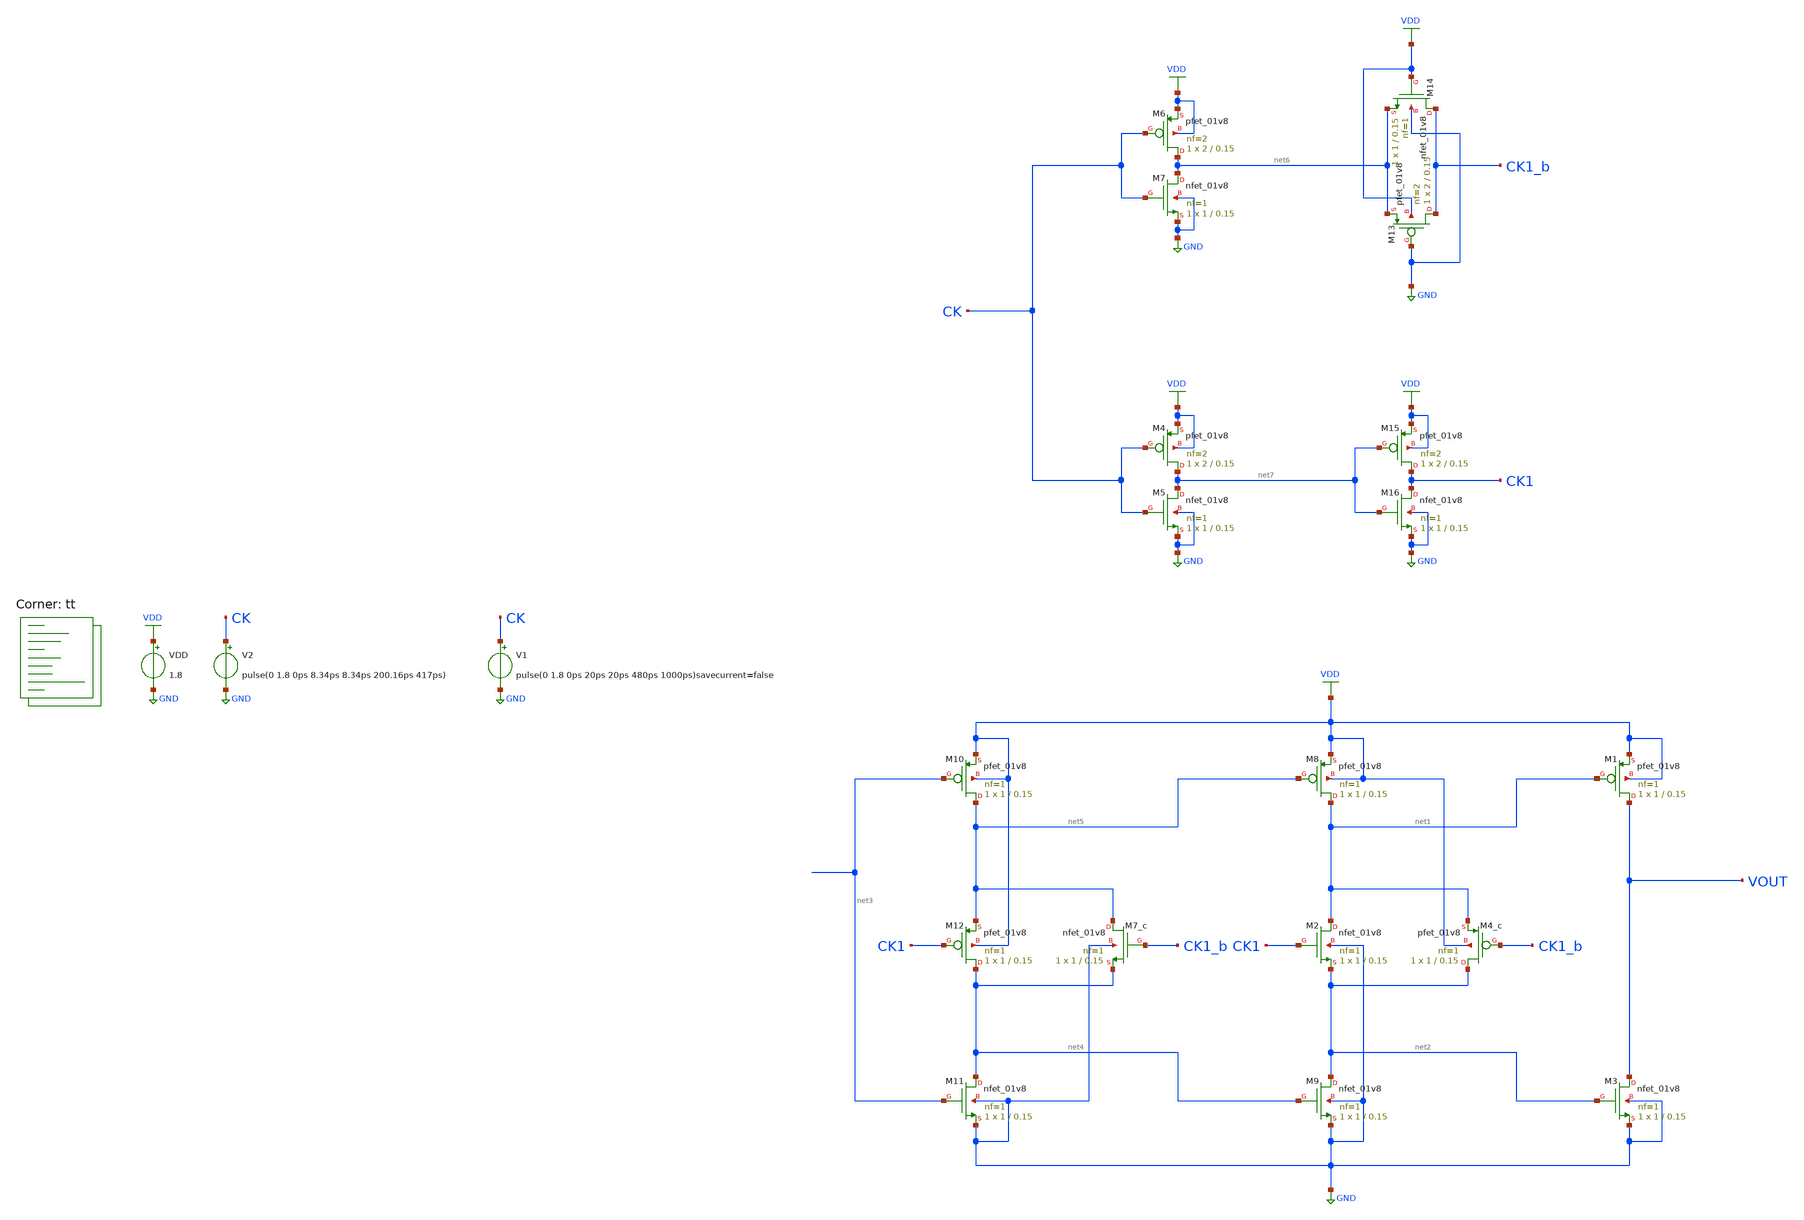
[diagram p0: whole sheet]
** sch_path: projects/pll/divider/xschem_ngspice/tb_FF_comp_sw_divide2_2.sch
**.subckt tb_FF_comp_sw_divide2_2
VDD VDD GND 1.8
V2 CK GND pulse(0 1.8 0ps 8.34ps 8.34ps 200.16ps 417ps)
XM1 VOUT net1 VDD VDD sky130_fd_pr__pfet_01v8 L=0.15 W=1 nf=1 ad='int((nf+1)/2) * W/nf * 0.29' as='int((nf+2)/2) * W/nf * 0.29'
+ pd='2*int((nf+1)/2) * (W/nf + 0.29)' ps='2*int((nf+2)/2) * (W/nf + 0.29)' nrd='0.29 / W' nrs='0.29 / W'
+ sa=0 sb=0 sd=0 mult=1 m=1
XM2 net1 CK1 net2 GND sky130_fd_pr__nfet_01v8 L=0.15 W=1 nf=1 ad='int((nf+1)/2) * W/nf * 0.29' as='int((nf+2)/2) * W/nf * 0.29'
+ pd='2*int((nf+1)/2) * (W/nf + 0.29)' ps='2*int((nf+2)/2) * (W/nf + 0.29)' nrd='0.29 / W' nrs='0.29 / W'
+ sa=0 sb=0 sd=0 mult=1 m=1
XM3 VOUT net2 GND GND sky130_fd_pr__nfet_01v8 L=0.15 W=1 nf=1 ad='int((nf+1)/2) * W/nf * 0.29' as='int((nf+2)/2) * W/nf * 0.29'
+ pd='2*int((nf+1)/2) * (W/nf + 0.29)' ps='2*int((nf+2)/2) * (W/nf + 0.29)' nrd='0.29 / W' nrs='0.29 / W'
+ sa=0 sb=0 sd=0 mult=1 m=1
XM8 net1 net5 VDD VDD sky130_fd_pr__pfet_01v8 L=0.15 W=1 nf=1 ad='int((nf+1)/2) * W/nf * 0.29' as='int((nf+2)/2) * W/nf * 0.29'
+ pd='2*int((nf+1)/2) * (W/nf + 0.29)' ps='2*int((nf+2)/2) * (W/nf + 0.29)' nrd='0.29 / W' nrs='0.29 / W'
+ sa=0 sb=0 sd=0 mult=1 m=1
XM9 net2 net4 GND GND sky130_fd_pr__nfet_01v8 L=0.15 W=1 nf=1 ad='int((nf+1)/2) * W/nf * 0.29' as='int((nf+2)/2) * W/nf * 0.29'
+ pd='2*int((nf+1)/2) * (W/nf + 0.29)' ps='2*int((nf+2)/2) * (W/nf + 0.29)' nrd='0.29 / W' nrs='0.29 / W'
+ sa=0 sb=0 sd=0 mult=1 m=1
XM10 net5 net3 VDD VDD sky130_fd_pr__pfet_01v8 L=0.15 W=1 nf=1 ad='int((nf+1)/2) * W/nf * 0.29' as='int((nf+2)/2) * W/nf * 0.29'
+ pd='2*int((nf+1)/2) * (W/nf + 0.29)' ps='2*int((nf+2)/2) * (W/nf + 0.29)' nrd='0.29 / W' nrs='0.29 / W'
+ sa=0 sb=0 sd=0 mult=1 m=1
XM11 net4 net3 GND GND sky130_fd_pr__nfet_01v8 L=0.15 W=1 nf=1 ad='int((nf+1)/2) * W/nf * 0.29' as='int((nf+2)/2) * W/nf * 0.29'
+ pd='2*int((nf+1)/2) * (W/nf + 0.29)' ps='2*int((nf+2)/2) * (W/nf + 0.29)' nrd='0.29 / W' nrs='0.29 / W'
+ sa=0 sb=0 sd=0 mult=1 m=1
XM12 net4 CK1 net5 VDD sky130_fd_pr__pfet_01v8 L=0.15 W=1 nf=1 ad='int((nf+1)/2) * W/nf * 0.29' as='int((nf+2)/2) * W/nf * 0.29'
+ pd='2*int((nf+1)/2) * (W/nf + 0.29)' ps='2*int((nf+2)/2) * (W/nf + 0.29)' nrd='0.29 / W' nrs='0.29 / W'
+ sa=0 sb=0 sd=0 mult=1 m=1
XM4_c net2 CK1_b net1 VDD sky130_fd_pr__pfet_01v8 L=0.15 W=1 nf=1 ad='int((nf+1)/2) * W/nf * 0.29' as='int((nf+2)/2) * W/nf * 0.29'
+ pd='2*int((nf+1)/2) * (W/nf + 0.29)' ps='2*int((nf+2)/2) * (W/nf + 0.29)' nrd='0.29 / W' nrs='0.29 / W'
+ sa=0 sb=0 sd=0 mult=1 m=1
XM7_c net5 CK1_b net4 GND sky130_fd_pr__nfet_01v8 L=0.15 W=1 nf=1 ad='int((nf+1)/2) * W/nf * 0.29' as='int((nf+2)/2) * W/nf * 0.29'
+ pd='2*int((nf+1)/2) * (W/nf + 0.29)' ps='2*int((nf+2)/2) * (W/nf + 0.29)' nrd='0.29 / W' nrs='0.29 / W'
+ sa=0 sb=0 sd=0 mult=1 m=1
XM13 CK1_b GND net6 VDD sky130_fd_pr__pfet_01v8 L=0.15 W=2 nf=2 ad='int((nf+1)/2) * W/nf * 0.29' as='int((nf+2)/2) * W/nf * 0.29'
+ pd='2*int((nf+1)/2) * (W/nf + 0.29)' ps='2*int((nf+2)/2) * (W/nf + 0.29)' nrd='0.29 / W' nrs='0.29 / W'
+ sa=0 sb=0 sd=0 mult=1 m=1
XM14 CK1_b VDD net6 GND sky130_fd_pr__nfet_01v8 L=0.15 W=1 nf=1 ad='int((nf+1)/2) * W/nf * 0.29' as='int((nf+2)/2) * W/nf * 0.29'
+ pd='2*int((nf+1)/2) * (W/nf + 0.29)' ps='2*int((nf+2)/2) * (W/nf + 0.29)' nrd='0.29 / W' nrs='0.29 / W'
+ sa=0 sb=0 sd=0 mult=1 m=1
XM15 CK1 net7 VDD VDD sky130_fd_pr__pfet_01v8 L=0.15 W=2 nf=2 ad='int((nf+1)/2) * W/nf * 0.29' as='int((nf+2)/2) * W/nf * 0.29'
+ pd='2*int((nf+1)/2) * (W/nf + 0.29)' ps='2*int((nf+2)/2) * (W/nf + 0.29)' nrd='0.29 / W' nrs='0.29 / W'
+ sa=0 sb=0 sd=0 mult=1 m=1
XM16 CK1 net7 GND GND sky130_fd_pr__nfet_01v8 L=0.15 W=1 nf=1 ad='int((nf+1)/2) * W/nf * 0.29' as='int((nf+2)/2) * W/nf * 0.29'
+ pd='2*int((nf+1)/2) * (W/nf + 0.29)' ps='2*int((nf+2)/2) * (W/nf + 0.29)' nrd='0.29 / W' nrs='0.29 / W'
+ sa=0 sb=0 sd=0 mult=1 m=1
XM4 net7 CK VDD VDD sky130_fd_pr__pfet_01v8 L=0.15 W=2 nf=2 ad='int((nf+1)/2) * W/nf * 0.29' as='int((nf+2)/2) * W/nf * 0.29'
+ pd='2*int((nf+1)/2) * (W/nf + 0.29)' ps='2*int((nf+2)/2) * (W/nf + 0.29)' nrd='0.29 / W' nrs='0.29 / W'
+ sa=0 sb=0 sd=0 mult=1 m=1
XM5 net7 CK GND GND sky130_fd_pr__nfet_01v8 L=0.15 W=1 nf=1 ad='int((nf+1)/2) * W/nf * 0.29' as='int((nf+2)/2) * W/nf * 0.29'
+ pd='2*int((nf+1)/2) * (W/nf + 0.29)' ps='2*int((nf+2)/2) * (W/nf + 0.29)' nrd='0.29 / W' nrs='0.29 / W'
+ sa=0 sb=0 sd=0 mult=1 m=1
XM6 net6 CK VDD VDD sky130_fd_pr__pfet_01v8 L=0.15 W=2 nf=2 ad='int((nf+1)/2) * W/nf * 0.29' as='int((nf+2)/2) * W/nf * 0.29'
+ pd='2*int((nf+1)/2) * (W/nf + 0.29)' ps='2*int((nf+2)/2) * (W/nf + 0.29)' nrd='0.29 / W' nrs='0.29 / W'
+ sa=0 sb=0 sd=0 mult=1 m=1
XM7 net6 CK GND GND sky130_fd_pr__nfet_01v8 L=0.15 W=1 nf=1 ad='int((nf+1)/2) * W/nf * 0.29' as='int((nf+2)/2) * W/nf * 0.29'
+ pd='2*int((nf+1)/2) * (W/nf + 0.29)' ps='2*int((nf+2)/2) * (W/nf + 0.29)' nrd='0.29 / W' nrs='0.29 / W'
+ sa=0 sb=0 sd=0 mult=1 m=1
V1 CK GND pulse(0 1.8 0ps 20ps 20ps 480ps 1000ps)savecurrent=false
**** begin user architecture code



.option method=gear
.option wnflag=1

.control

  save all
  tran 5p 100n
  remzerovec
  write tb_FF_comp_sw.raw
  * set appendwrite

.endc



.lib $::SKYWATER_MODELS/sky130.lib.spice tt
**** end user architecture code
**.ends
.GLOBAL GND
.GLOBAL VDD
.end
